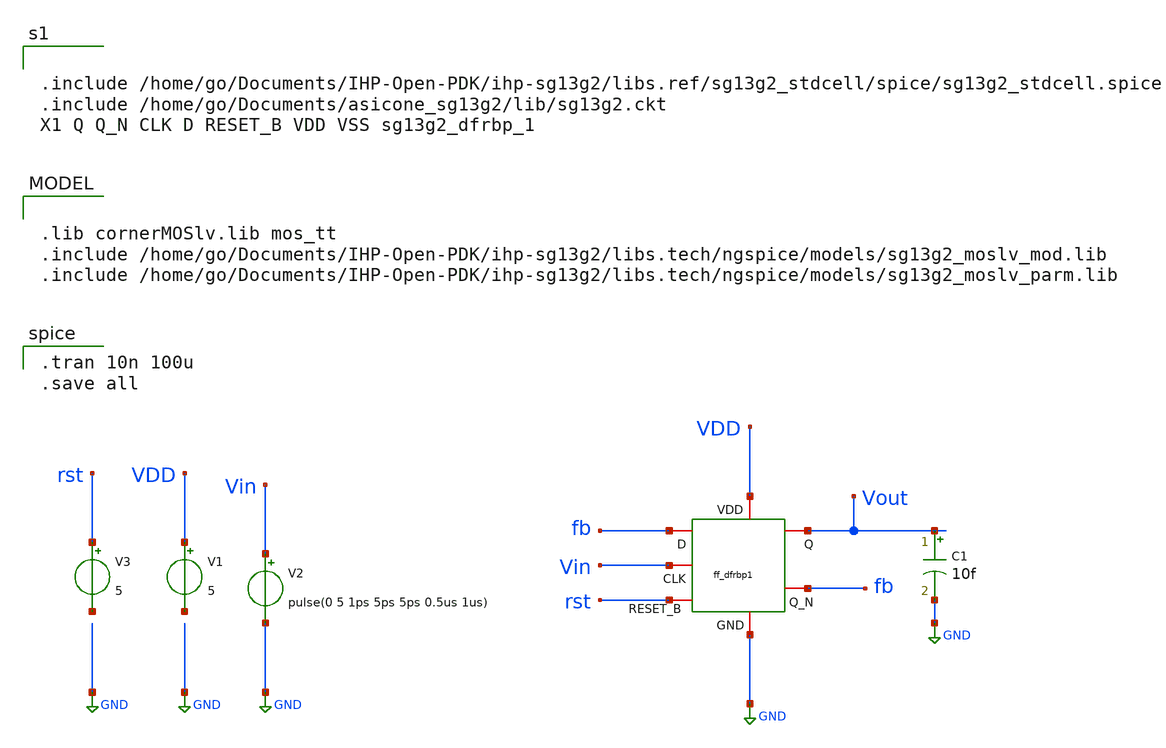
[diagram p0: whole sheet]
** sch_path: unic_cass_wrapper_user_project/ROs_reliability/div_stdcell_tb.sch
**.subckt div_stdcell_tb
V1 VDD net1 5
V2 Vin GND pulse(0 5 1ps 5ps 5ps 0.5us 1us)
V3 rst net2 5
C1 Vout GND 10f m=1
**** begin user architecture code

.tran 10n 100u
.save all


.lib cornerMOSlv.lib mos_tt
.include /home/go/Documents/IHP-Open-PDK/ihp-sg13g2/libs.tech/ngspice/models/sg13g2_moslv_mod.lib
.include /home/go/Documents/IHP-Open-PDK/ihp-sg13g2/libs.tech/ngspice/models/sg13g2_moslv_parm.lib



.include /home/go/Documents/IHP-Open-PDK/ihp-sg13g2/libs.ref/sg13g2_stdcell/spice/sg13g2_stdcell.spice
.include /home/go/Documents/asicone_sg13g2/lib/sg13g2.ckt
X1 Q Q_N CLK D RESET_B VDD VSS sg13g2_dfrbp_1


**** end user architecture code
**.ends
.GLOBAL GND
.end
